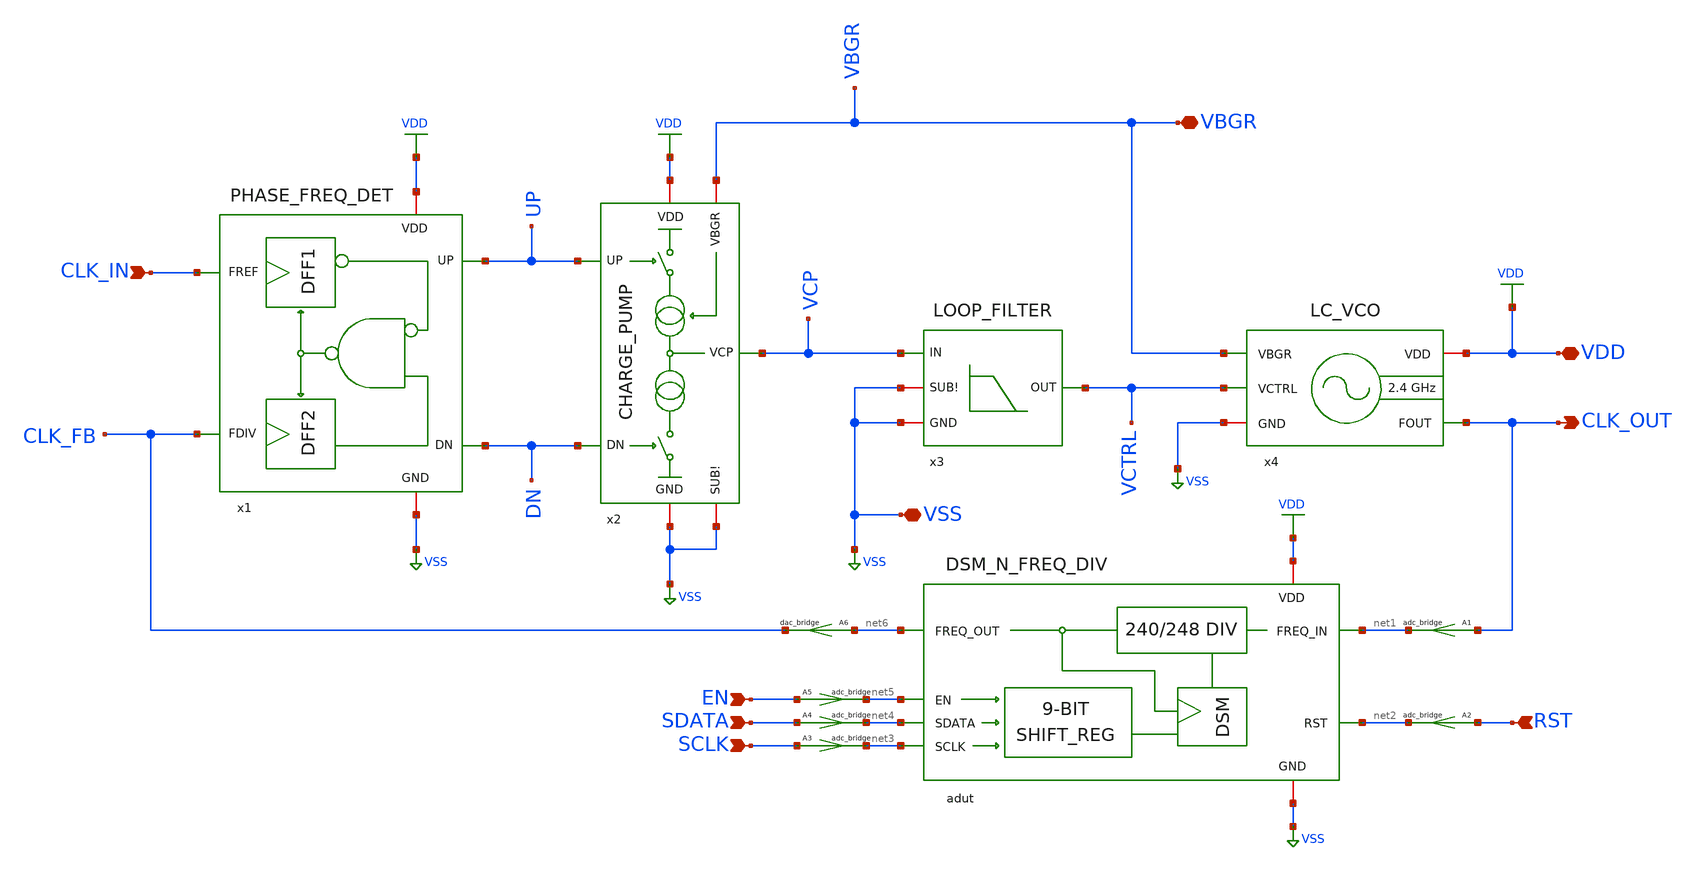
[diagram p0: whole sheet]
** sch_path: xschem/top-pll/LC_VCO_FPLL.sch
**.subckt LC_VCO_FPLL CLK_IN CLK_OUT EN SDATA SCLK RST VDD VSS VBGR
*.ipin CLK_IN
*.opin CLK_OUT
*.ipin EN
*.ipin SDATA
*.ipin SCLK
*.ipin RST
*.iopin VDD
*.iopin VSS
*.iopin VBGR
x1 CLK_IN UP VDD VSS CLK_FB DN PHASE_FREQ_DET
x2 UP VDD VCP VBGR VSS DN VSS CHARGE_PUMP
x3 VCTRL VCP VSS VSS LOOP_FILTER
x4 VDD VCTRL VSS CLK_OUT VBGR LC_VCO
adut [ net1 net2 net3 net4 net5 ] [ net6 ] null dut
.model dut d_cosim simulation=../simulations/dsm_and_freq_divider.so
A1 [ CLK_OUT ] [ net1 ] adc1
.model adc1 adc_bridge in_low=0.76 in_high=0.76
A2 [ RST ] [ net2 ] adc1
.model adc1 adc_bridge in_low=0.76 in_high=0.76
A3 [ SCLK ] [ net3 ] adc1
.model adc1 adc_bridge in_low=0.76 in_high=0.76
A4 [ SDATA ] [ net4 ] adc1
.model adc1 adc_bridge in_low=0.76 in_high=0.76
A5 [ EN ] [ net5 ] adc1
.model adc1 adc_bridge in_low=0.76 in_high=0.76
A6 [ net6 ] [ CLK_FB ] dac1
.model dac1 dac_bridge out_low=0 out_high=1.2
**.ends
.GLOBAL VSS
.GLOBAL VDD
.end
